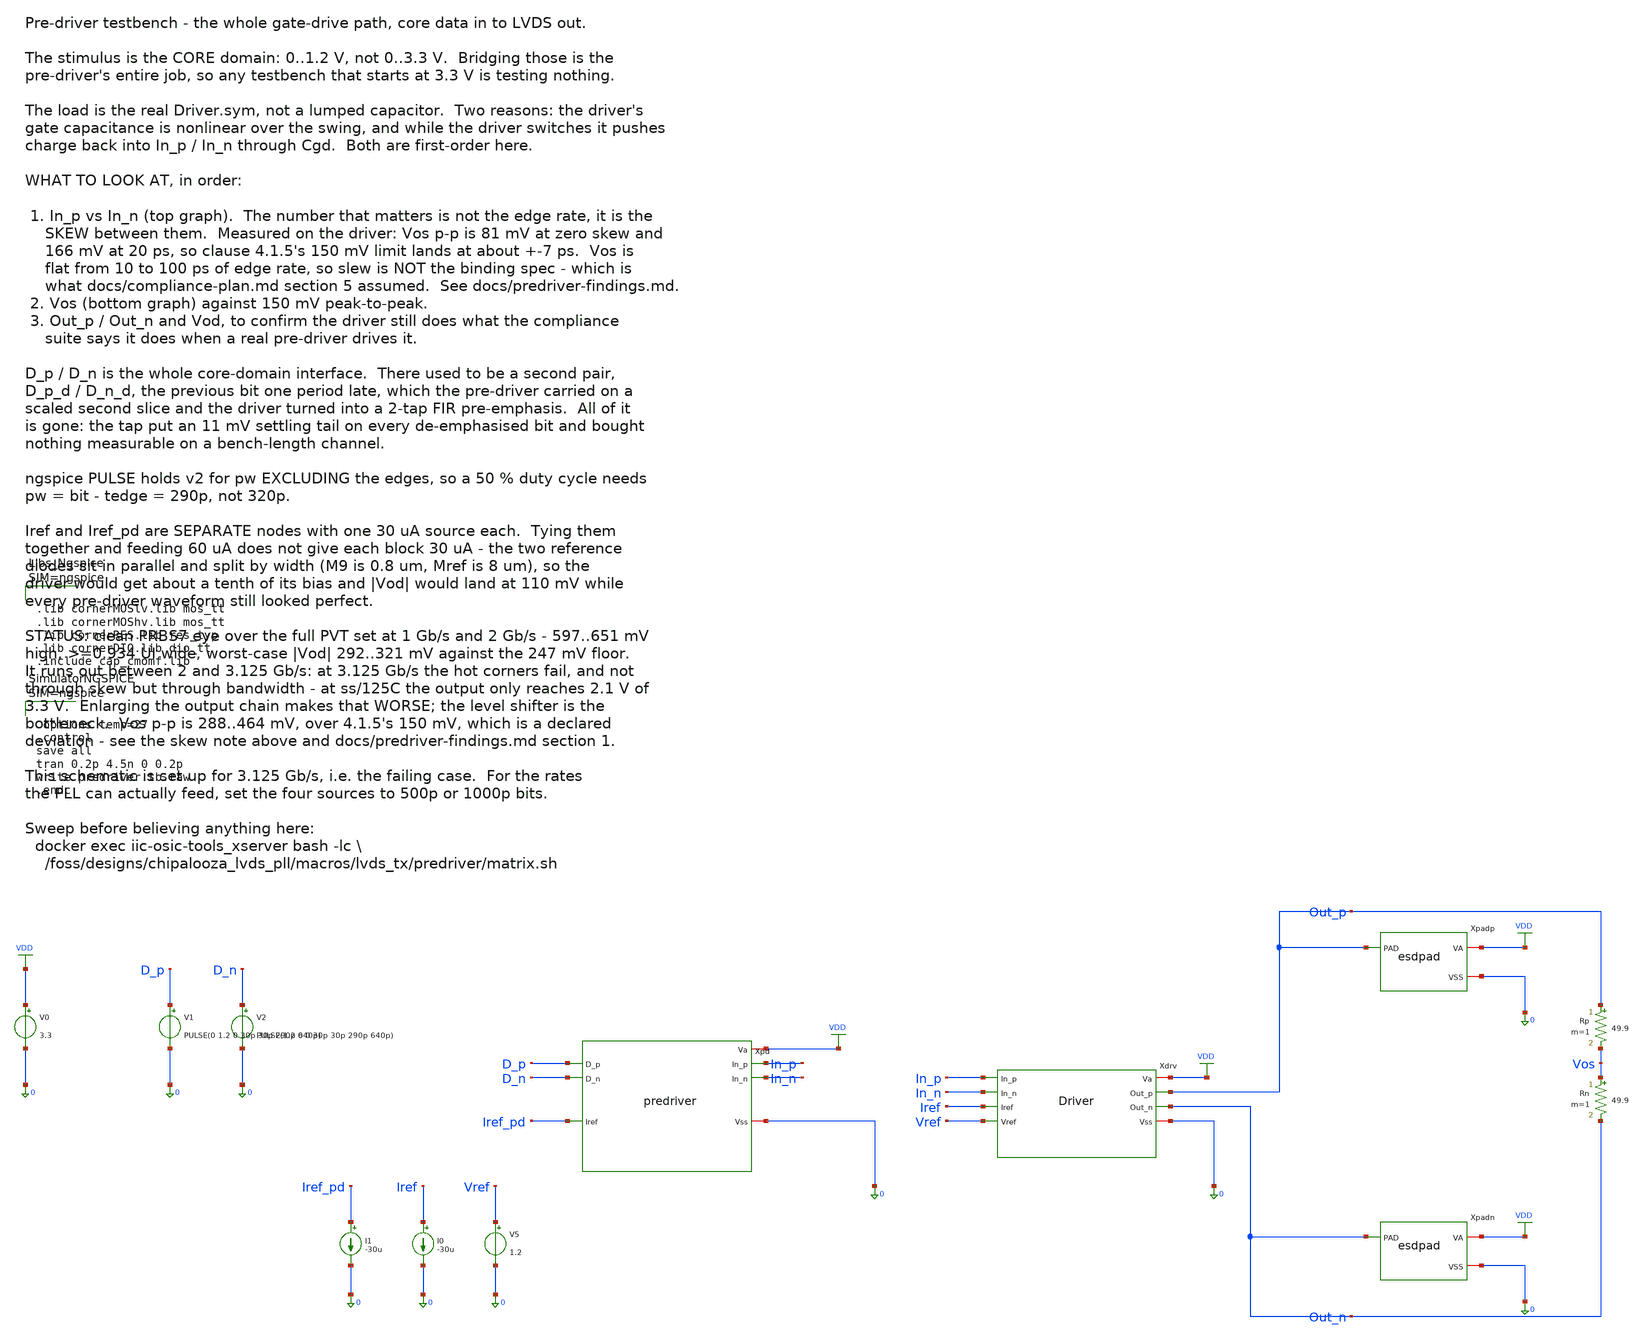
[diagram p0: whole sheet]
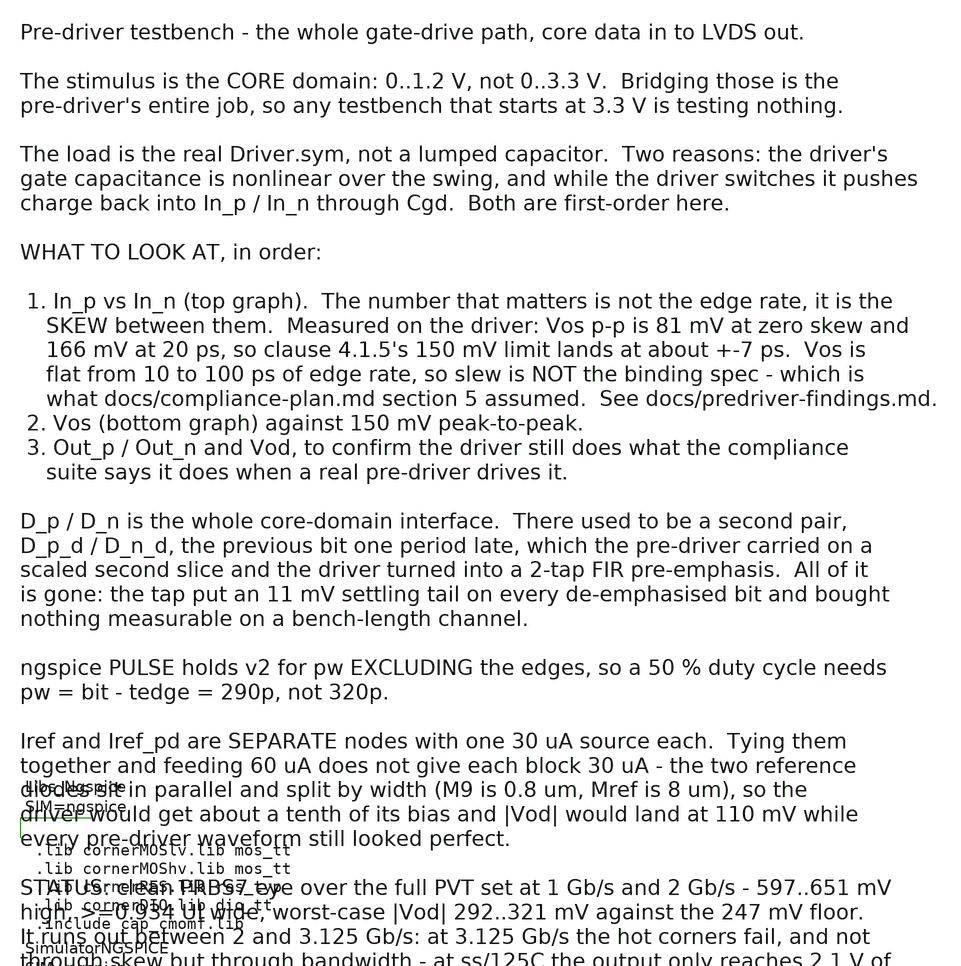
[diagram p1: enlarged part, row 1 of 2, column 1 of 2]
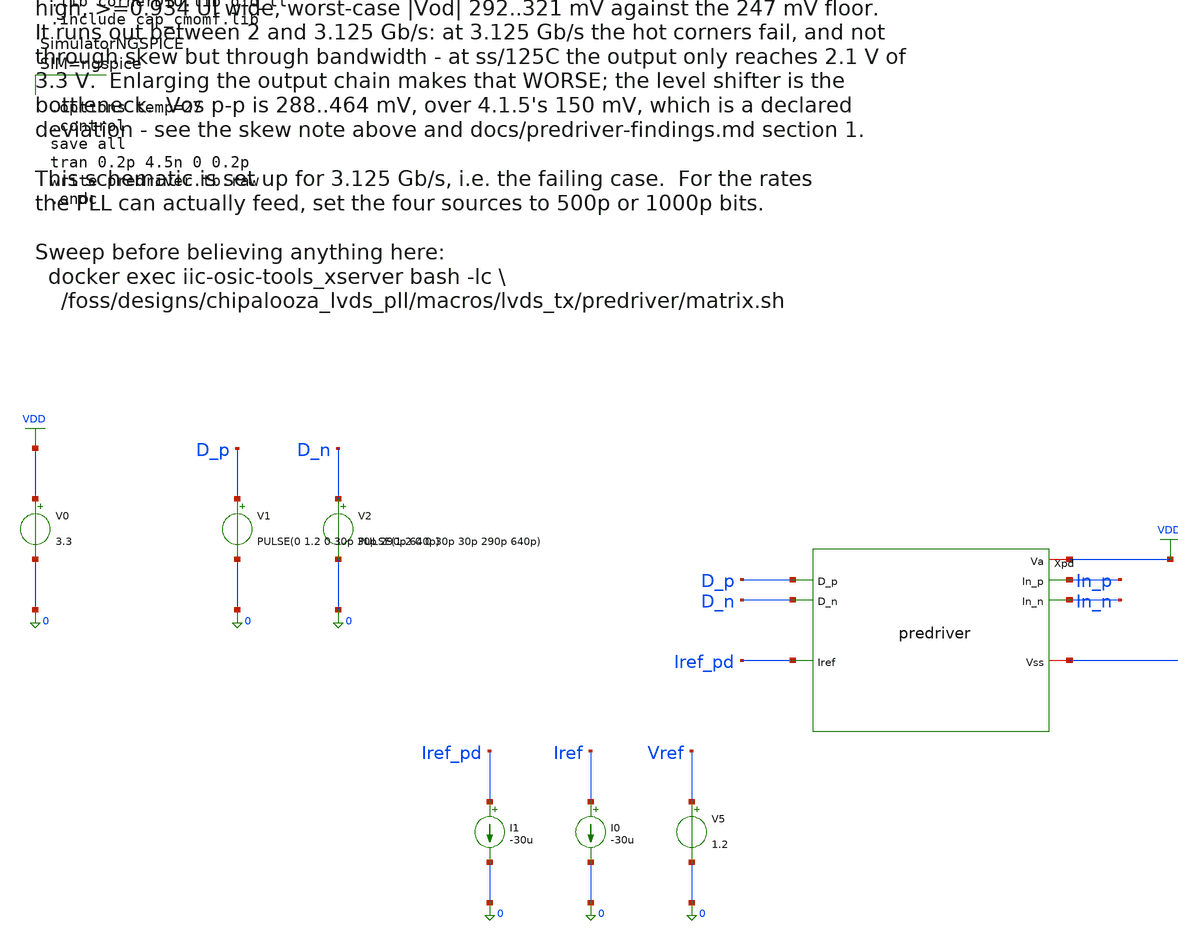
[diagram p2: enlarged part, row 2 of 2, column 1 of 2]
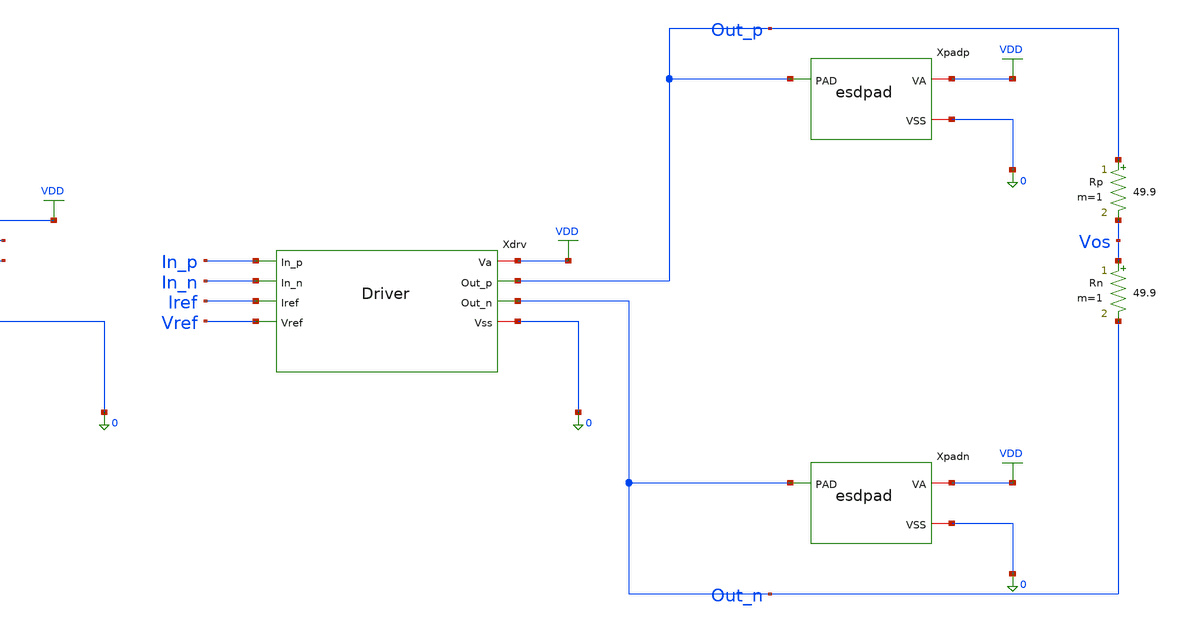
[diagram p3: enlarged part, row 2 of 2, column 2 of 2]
** sch_path: macros/lvds_tx/testbenches/xschem/predriver.tb.sch
**.subckt predriver.tb
Xpd D_p D_n Iref_pd In_p In_n VDD 0 predriver
Xdrv VDD Out_p In_p In_n Iref Vref Out_n 0 Driver
Xpadp Out_p VDD 0 esdpad
Xpadn Out_n VDD 0 esdpad
V0 VDD 0 3.3
V1 D_p 0 PULSE(0 1.2 0 30p 30p 290p 640p)
V2 D_n 0 PULSE(1.2 0 0 30p 30p 290p 640p)
V5 Vref 0 1.2
I0 Iref 0 -30u
I1 Iref_pd 0 -30u
Rp Out_p Vos 49.9 m=1
Rn Vos Out_n 49.9 m=1
**** begin user architecture code



.lib cornerMOSlv.lib mos_tt
.lib cornerMOShv.lib mos_tt
.lib cornerRES.lib res_typ
.lib cornerDIO.lib dio_tt
.include cap_cmomf.lib






.options temp=27
.control
save all
tran 0.2p 4.5n 0 0.2p
write predriver.tb.raw
.endc



**** end user architecture code
**.ends

* expanding   symbol:  predriver.sym # of pins=7
** sym_path: macros/lvds_tx/schematic/xschem/predriver.sym
** sch_path: macros/lvds_tx/schematic/xschem/predriver.sch
.subckt predriver D_p D_n Iref In_p In_n Va Vss
*.iopin Va
*.iopin Vss
*.ipin Iref
*.ipin D_p
*.ipin D_n
*.opin In_p
*.opin In_n
Xkpm D_p D_n Iref net1 Va Vss predriver_comp
XMref Iref Iref Vss Vss sg13_hv_nmos w=2u l=2u ng=1 m=1 mm_ok=1
Xknm D_n D_p Iref net2 Va Vss predriver_comp
Xstm net1 net2 In_p In_n Va Vss predriver_stage
.ends


* expanding   symbol:  Driver.sym # of pins=8
** sym_path: macros/lvds_tx/schematic/xschem/Driver.sym
** sch_path: macros/lvds_tx/schematic/xschem/Driver.sch
.subckt Driver Va Out_p In_p In_n Iref Vref Out_n Vss
*.iopin Va
*.iopin Vss
*.opin Out_p
*.opin Out_n
*.ipin In_p
*.ipin In_n
*.ipin Iref
*.ipin Vref
XM2 tail_p cmfb Va Va sg13_hv_pmos w=97.2u l=0.5u ng=12 m=1 mm_ok=1
XM5 Out_p In_p tail_p Va sg13_hv_pmos w=80u l=0.4u ng=40 m=1 mm_ok=1
XM4 Out_n In_n tail_p Va sg13_hv_pmos w=80u l=0.4u ng=40 m=1 mm_ok=1
XM1 Out_p In_p tail_n Vss sg13_hv_nmos w=30u l=0.45u ng=15 m=1 mm_ok=1
XM3 Out_n In_n tail_n Vss sg13_hv_nmos w=30u l=0.45u ng=15 m=1 mm_ok=1
XM6 tail_n Iref Vss Vss sg13_hv_nmos w=24.8u l=0.5u ng=31 m=4 mm_ok=1
XM9 Iref Iref Vss Vss sg13_hv_nmos w=0.8u l=0.5u ng=1 m=1 mm_ok=1
XM13 pd pd Va Va sg13_hv_pmos w=5u l=1u ng=1 m=1 mm_ok=1
XM14 cmfb pd Va Va sg13_hv_pmos w=5u l=1u ng=1 m=1 mm_ok=1
XM11 pd cm otail Vss sg13_hv_nmos w=40u l=1u ng=20 m=1 mm_ok=1
XM12 cmfb Vref otail Vss sg13_hv_nmos w=40u l=1u ng=20 m=1 mm_ok=1
XM10 otail Iref Vss Vss sg13_hv_nmos w=0.8u l=0.5u ng=1 m=1 mm_ok=1
XCc Va cmfb Va Va sg13_hv_pmos w=40u l=5u ng=8 m=1 mm_ok=1
XRp Out_p cm Vss rhigh w=1u l=7.35u m=1 b=0 mm_ok=1
XRn Out_n cm Vss rhigh w=1u l=7.35u m=1 b=0 mm_ok=1
XCxp Out_p In_n cap_cmomf w=5.913u l=5.913u mmin=1 mmax=4 subblock=0 rfmodel=0 subscale=1 m=1
+ mm_ok=1
XCxn Out_n In_p cap_cmomf w=5.913u l=5.913u mmin=1 mmax=4 subblock=0 rfmodel=0 subscale=1 m=1
+ mm_ok=1
XCop Vss Out_p Vss Vss sg13_hv_nmos w=10.0u l=10.0u ng=1 m=1 mm_ok=1
XCon Vss Out_n Vss Vss sg13_hv_nmos w=10.0u l=10.0u ng=1 m=1 mm_ok=1
.ends


* expanding   symbol:  esdpad.sym # of pins=3
** sym_path: macros/lvds_tx/schematic/xschem/esdpad.sym
** sch_path: macros/lvds_tx/schematic/xschem/esdpad.sch
.subckt esdpad PAD VA VSS
*.iopin PAD
*.iopin VA
*.iopin VSS
XDdvdd VA PAD VSS diodevdd_4kv m=1
XDdvss VA PAD VSS diodevss_4kv m=1
Cpad PAD VSS 90f m=1
.ends


* expanding   symbol:  predriver_comp.sym # of pins=6
** sym_path: macros/lvds_tx/schematic/xschem/predriver_comp.sym
** sch_path: macros/lvds_tx/schematic/xschem/predriver_comp.sch
.subckt predriver_comp Gin Din Iref Out Va Vss
*.iopin Va
*.iopin Vss
*.opin Out
*.ipin Din
*.ipin Gin
*.ipin Iref
XMld net1 net1 Va Va sg13_hv_pmos w=12u l=0.4u ng=4 m=1 mm_ok=1
XMlo Out net1 Va Va sg13_hv_pmos w=12u l=0.4u ng=4 m=1 mm_ok=1
XMid net1 Din net2 Vss sg13_hv_nmos w=24u l=0.45u ng=6 m=1 mm_ok=1
XMio Out Gin net2 Vss sg13_hv_nmos w=24u l=0.45u ng=6 m=1 mm_ok=1
XMt net2 Iref Vss Vss sg13_hv_nmos w=17.52u l=0.45u ng=6 m=2 mm_ok=1
.ends


* expanding   symbol:  predriver_stage.sym # of pins=6
** sym_path: macros/lvds_tx/schematic/xschem/predriver_stage.sym
** sch_path: macros/lvds_tx/schematic/xschem/predriver_stage.sch
.subckt predriver_stage In_p In_n Out_p Out_n Va Vss
*.ipin In_p
*.opin Out_p
*.ipin In_n
*.opin Out_n
*.iopin Va
*.iopin Vss
XMpp0 net1 In_p Va Va sg13_hv_pmos w=2.64u l=0.4u ng=1 m=1 mm_ok=1
XMnp0 net1 In_p Vss Vss sg13_hv_nmos w=1.6u l=0.45u ng=1 m=1 mm_ok=1
XMpp1 net2 net1 Va Va sg13_hv_pmos w=12.52u l=0.4u ng=4 m=1 mm_ok=1
XMnp1 net2 net1 Vss Vss sg13_hv_nmos w=5u l=0.45u ng=4 m=1 mm_ok=1
XMpp2 Out_p net2 Va Va sg13_hv_pmos w=40u l=0.4u ng=10 m=1 mm_ok=1
XMnp2 Out_p net2 Vss Vss sg13_hv_nmos w=16u l=0.45u ng=10 m=1 mm_ok=1
XMpn0 net3 In_n Va Va sg13_hv_pmos w=2.64u l=0.4u ng=1 m=1 mm_ok=1
XMnn0 net3 In_n Vss Vss sg13_hv_nmos w=1.6u l=0.45u ng=1 m=1 mm_ok=1
XMpn1 net4 net3 Va Va sg13_hv_pmos w=12.52u l=0.4u ng=4 m=1 mm_ok=1
XMnn1 net4 net3 Vss Vss sg13_hv_nmos w=5u l=0.45u ng=4 m=1 mm_ok=1
XMpn2 Out_n net4 Va Va sg13_hv_pmos w=40u l=0.4u ng=10 m=1 mm_ok=1
XMnn2 Out_n net4 Vss Vss sg13_hv_nmos w=16u l=0.45u ng=10 m=1 mm_ok=1
XMpxp net4 net2 Va Va sg13_hv_pmos w=4.38u l=0.4u ng=1 m=1 mm_ok=1
XMnxp net4 net2 Vss Vss sg13_hv_nmos w=1.75u l=0.45u ng=1 m=1 mm_ok=1
XMpxn net2 net4 Va Va sg13_hv_pmos w=4.38u l=0.4u ng=1 m=1 mm_ok=1
XMnxn net2 net4 Vss Vss sg13_hv_nmos w=1.75u l=0.45u ng=1 m=1 mm_ok=1
.ends

.GLOBAL VDD
.end
